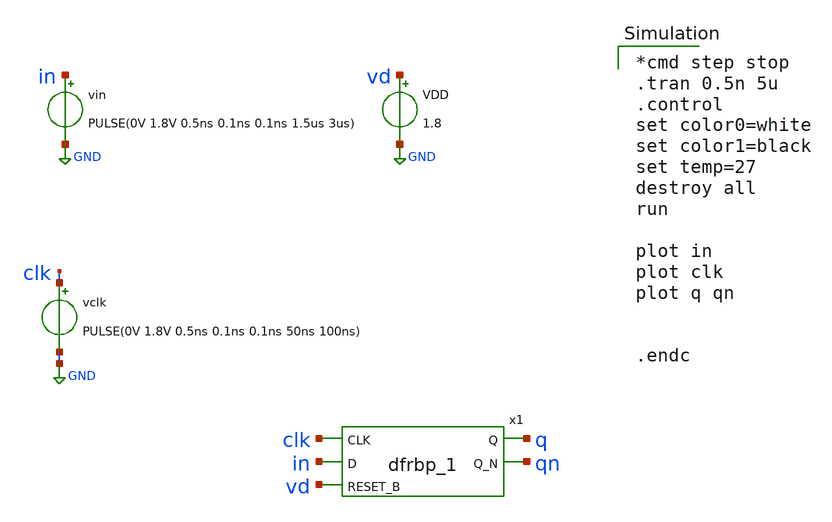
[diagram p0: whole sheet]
** sch_path: sigma-delta_modulator/xschem/dff_tb-tran.sch
* Copyright 2020 Stefan Frederik Schippers
* Licensed under the Apache License, Version 2.0 (the "License");
* you may not use this file except in compliance with the License.
* You may obtain a copy of the License at
* https://www.apache.org/licenses/LICENSE-2.0
* Unless required by applicable law or agreed to in writing, software
* distributed under the License is distributed on an "AS IS" BASIS,
* WITHOUT WARRANTIES OR CONDITIONS OF ANY KIND, either express or implied.
* See the License for the specific language governing permissions and
* limitations under the License.
**.subckt dff_tb-tran
vclk clk GND PULSE(0V 1.8V 0.5ns 0.1ns 0.1ns 50ns 100ns)
VDD vd GND 1.8
vin in GND PULSE(0V 1.8V 0.5ns 0.1ns 0.1ns 1.5us 3us)
x1 clk in vd GND GND VD VD q qn sky130_fd_sc_hd__dfrbp_1
**** begin user architecture code

*cmd step stop
.tran 0.5n 5u
.control
set color0=white
set color1=black
set temp=27
destroy all
run

plot in
plot clk
plot q qn


.endc

 .lib $::SKYWATER_MODELS/sky130.lib.spice tt
.include $::SKYWATER_STDCELLS/sky130_fd_sc_hd.spice

**** end user architecture code
**.ends
.GLOBAL GND
.end
